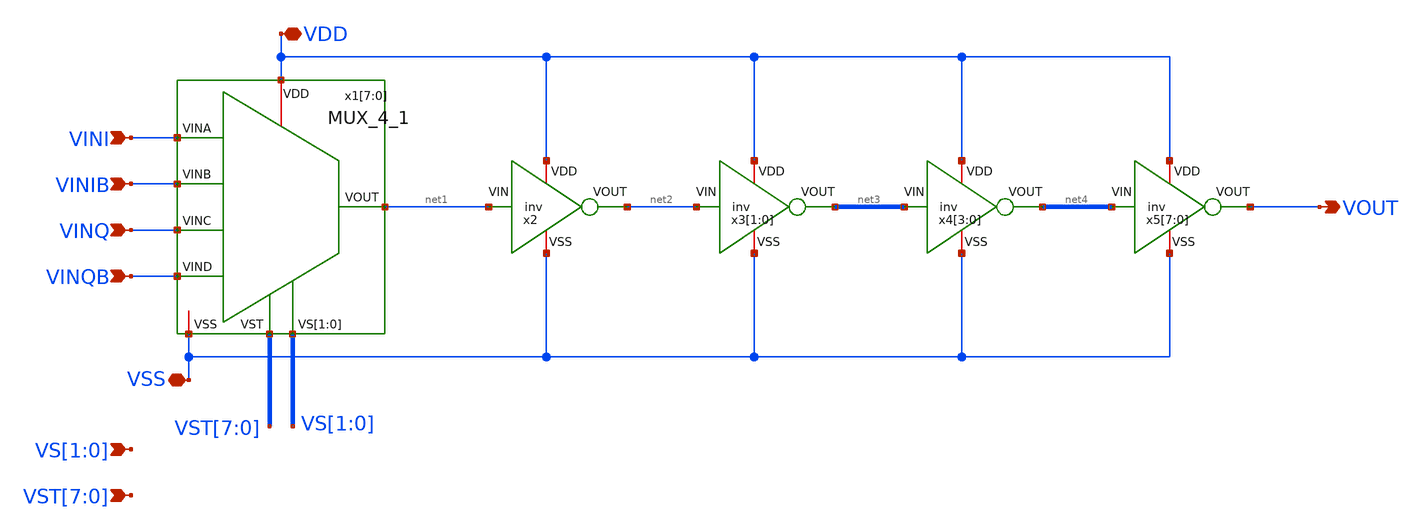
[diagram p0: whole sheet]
** sch_path: 8xPI/8xPI.sch
**.subckt 8xPI VINI VINQ VINIB VINQB VDD VSS VOUT VS[1],VS[0]
*+ VST[7],VST[6],VST[5],VST[4],VST[3],VST[2],VST[1],VST[0]
*.ipin VINI
*.ipin VINQ
*.ipin VINIB
*.ipin VINQB
*.iopin VDD
*.iopin VSS
*.opin VOUT
*.ipin VS[1],VS[0]
*.ipin VST[7],VST[6],VST[5],VST[4],VST[3],VST[2],VST[1],VST[0]
x1[7] VINI VINIB VDD net1 VS[1] VS[0] VINQ VSS VINQB VST[7] MUX_4_1
x1[6] VINI VINIB VDD net1 VS[1] VS[0] VINQ VSS VINQB VST[6] MUX_4_1
x1[5] VINI VINIB VDD net1 VS[1] VS[0] VINQ VSS VINQB VST[5] MUX_4_1
x1[4] VINI VINIB VDD net1 VS[1] VS[0] VINQ VSS VINQB VST[4] MUX_4_1
x1[3] VINI VINIB VDD net1 VS[1] VS[0] VINQ VSS VINQB VST[3] MUX_4_1
x1[2] VINI VINIB VDD net1 VS[1] VS[0] VINQ VSS VINQB VST[2] MUX_4_1
x1[1] VINI VINIB VDD net1 VS[1] VS[0] VINQ VSS VINQB VST[1] MUX_4_1
x1[0] VINI VINIB VDD net1 VS[1] VS[0] VINQ VSS VINQB VST[0] MUX_4_1
x2 VDD net2 net1 VSS inv
x3[1] VDD net3[1] net2 VSS inv
x3[0] VDD net3[0] net2 VSS inv
x4[3] VDD net4[3] net3[1] VSS inv
x4[2] VDD net4[2] net3[0] VSS inv
x4[1] VDD net4[1] net3[1] VSS inv
x4[0] VDD net4[0] net3[0] VSS inv
x5[7] VDD VOUT net4[3] VSS inv
x5[6] VDD VOUT net4[2] VSS inv
x5[5] VDD VOUT net4[1] VSS inv
x5[4] VDD VOUT net4[0] VSS inv
x5[3] VDD VOUT net4[3] VSS inv
x5[2] VDD VOUT net4[2] VSS inv
x5[1] VDD VOUT net4[1] VSS inv
x5[0] VDD VOUT net4[0] VSS inv
**.ends

* expanding   symbol:  /foss/designs/PhaseInterpolator/Custom_std_cells/MUX_4_1.sym # of pins=9
** sym_path: /foss/designs/PhaseInterpolator/Custom_std_cells/MUX_4_1.sym
** sch_path: /foss/designs/PhaseInterpolator/Custom_std_cells/MUX_4_1.sch
.subckt MUX_4_1 VINA VINB VDD VOUT VS[1] VS[0] VINC VSS VIND VST
*.opin VOUT
*.iopin VDD
*.iopin VSS
*.ipin VINA
*.ipin VINB
*.ipin VINC
*.ipin VIND
*.ipin VS[1],VS[0]
*.ipin VST
x3 VDD VINC net2 VS[1] VIND VSS MUX_2_1
x4 VDD VINA net1 VS[0] VINB VSS MUX_2_1
x5 VDD net1 VOUT VST net2 VSS MUX_2_1
.ends


* expanding   symbol:  /foss/designs/PhaseInterpolator/Custom_std_cells/MUX_2_1.sym # of pins=6
** sym_path: /foss/designs/PhaseInterpolator/Custom_std_cells/MUX_2_1.sym
** sch_path: /foss/designs/PhaseInterpolator/Custom_std_cells/MUX_2_1.sch
.subckt MUX_2_1 VDD VINA VOUT VS VINB VSS
*.opin VOUT
*.ipin VINA
*.ipin VINB
*.ipin VS
*.iopin VDD
*.iopin VSS
x1 VOUT net1 VS VINA VDD VSS tg_custom
x2 VOUT VS net1 VINB VDD VSS tg_custom
x3 VDD net1 VS VSS inv
.ends


* expanding   symbol:  /foss/designs/PhaseInterpolator/Custom_std_cells/tg_custom.sym # of pins=6
** sym_path: /foss/designs/PhaseInterpolator/Custom_std_cells/tg_custom.sym
** sch_path: /foss/designs/PhaseInterpolator/Custom_std_cells/tg_custom.sch
.subckt tg_custom VOUT VSN VSP VIN VBP VBN
*.iopin VIN
*.iopin VSN
*.iopin VOUT
*.iopin VSP
*.iopin VBN
*.iopin VBP
XM1 VOUT VSN VIN VBN sg13_lv_nmos w=0.15u l=0.13u ng=1 m=1 mm_ok=1
XM2 VOUT VSP VIN VBP sg13_lv_pmos w=0.15u l=0.13u ng=1 m=2 mm_ok=1
.ends

.end
